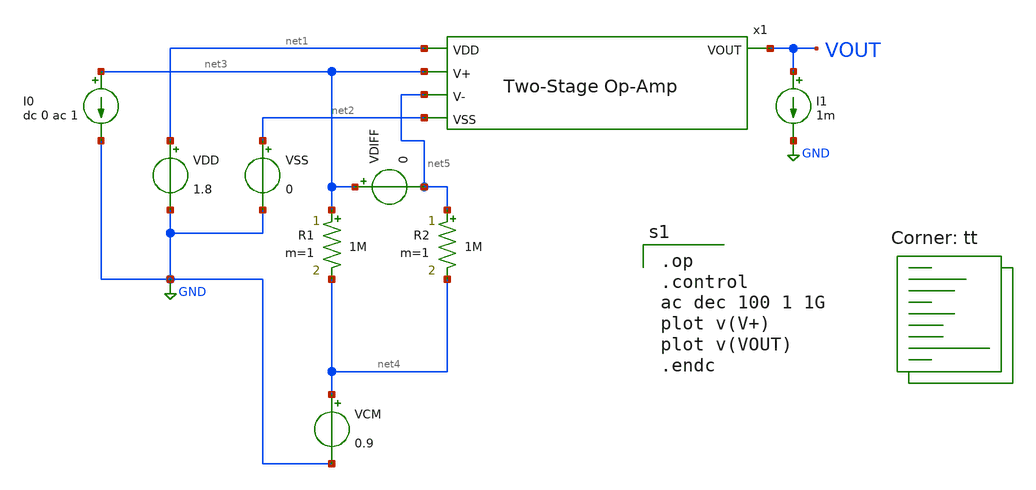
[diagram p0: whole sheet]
** sch_path: analog/schematics/tb_impedance.sch
**.subckt tb_impedance
VDD net1 GND 1.8
VSS net2 GND 0
VCM net4 GND 0.9
VDIFF net3 net5 0
R1 net3 net4 1M m=1
R2 net5 net4 1M m=1
x1 net1 net3 net5 VOUT net2 bootcamp_opamp
I0 net3 GND dc 0 ac 1
I1 VOUT GND 1m
**** begin user architecture code

.op
.control
ac dec 100 1 1G
plot v(V+)
plot v(VOUT)
.endc

.lib $::SKYWATER_MODELS/sky130.lib.spice tt
**** end user architecture code
**.ends

* expanding   symbol:  bootcamp_opamp.sym # of pins=5
** sym_path: analog/schematics/bootcamp_opamp.sym
** sch_path: analog/schematics/bootcamp_opamp.sch
.subckt bootcamp_opamp VDD V+ V- VOUT VSS
*.ipin V+
*.ipin V-
*.opin VOUT
*.ipin VDD
*.ipin VSS
XM1 net1 V+ net3 VSS sky130_fd_pr__nfet_01v8 L=1 W=4 nf=1 ad='int((nf+1)/2) * W/nf * 0.29' as='int((nf+2)/2) * W/nf * 0.29'
+ pd='2*int((nf+1)/2) * (W/nf + 0.29)' ps='2*int((nf+2)/2) * (W/nf + 0.29)' nrd='0.29 / W' nrs='0.29 / W'
+ sa=0 sb=0 sd=0 mult=1 m=1
XM2 net2 V- net3 VSS sky130_fd_pr__nfet_01v8 L=1 W=4 nf=1 ad='int((nf+1)/2) * W/nf * 0.29' as='int((nf+2)/2) * W/nf * 0.29'
+ pd='2*int((nf+1)/2) * (W/nf + 0.29)' ps='2*int((nf+2)/2) * (W/nf + 0.29)' nrd='0.29 / W' nrs='0.29 / W'
+ sa=0 sb=0 sd=0 mult=1 m=1
XM3 net1 net1 VDD VDD sky130_fd_pr__pfet_01v8 L=1 W=4 nf=1 ad='int((nf+1)/2) * W/nf * 0.29' as='int((nf+2)/2) * W/nf * 0.29'
+ pd='2*int((nf+1)/2) * (W/nf + 0.29)' ps='2*int((nf+2)/2) * (W/nf + 0.29)' nrd='0.29 / W' nrs='0.29 / W'
+ sa=0 sb=0 sd=0 mult=1 m=1
XM4 net2 net1 VDD VDD sky130_fd_pr__pfet_01v8 L=1 W=4 nf=1 ad='int((nf+1)/2) * W/nf * 0.29' as='int((nf+2)/2) * W/nf * 0.29'
+ pd='2*int((nf+1)/2) * (W/nf + 0.29)' ps='2*int((nf+2)/2) * (W/nf + 0.29)' nrd='0.29 / W' nrs='0.29 / W'
+ sa=0 sb=0 sd=0 mult=1 m=1
XM5 net3 net4 VSS VSS sky130_fd_pr__nfet_01v8 L=0.5 W=4 nf=1 ad='int((nf+1)/2) * W/nf * 0.29' as='int((nf+2)/2) * W/nf * 0.29'
+ pd='2*int((nf+1)/2) * (W/nf + 0.29)' ps='2*int((nf+2)/2) * (W/nf + 0.29)' nrd='0.29 / W' nrs='0.29 / W'
+ sa=0 sb=0 sd=0 mult=1 m=1
XM6 net4 net4 VSS VSS sky130_fd_pr__nfet_01v8 L=0.5 W=4 nf=1 ad='int((nf+1)/2) * W/nf * 0.29' as='int((nf+2)/2) * W/nf * 0.29'
+ pd='2*int((nf+1)/2) * (W/nf + 0.29)' ps='2*int((nf+2)/2) * (W/nf + 0.29)' nrd='0.29 / W' nrs='0.29 / W'
+ sa=0 sb=0 sd=0 mult=1 m=1
XM8 VOUT net4 VSS VSS sky130_fd_pr__nfet_01v8 L=0.5 W=2 nf=1 ad='int((nf+1)/2) * W/nf * 0.29' as='int((nf+2)/2) * W/nf * 0.29'
+ pd='2*int((nf+1)/2) * (W/nf + 0.29)' ps='2*int((nf+2)/2) * (W/nf + 0.29)' nrd='0.29 / W' nrs='0.29 / W'
+ sa=0 sb=0 sd=0 mult=1 m=1
XC1 net2 VOUT sky130_fd_pr__cap_mim_m3_1 W=22 L=22 MF=1 m=1
R1 VDD net4 12k m=1
XM7 VOUT net2 VDD VDD sky130_fd_pr__pfet_01v8 L=0.5 W=8 nf=1 ad='int((nf+1)/2) * W/nf * 0.29' as='int((nf+2)/2) * W/nf * 0.29'
+ pd='2*int((nf+1)/2) * (W/nf + 0.29)' ps='2*int((nf+2)/2) * (W/nf + 0.29)' nrd='0.29 / W' nrs='0.29 / W'
+ sa=0 sb=0 sd=0 mult=1 m=1
.ends

.GLOBAL GND
.end
